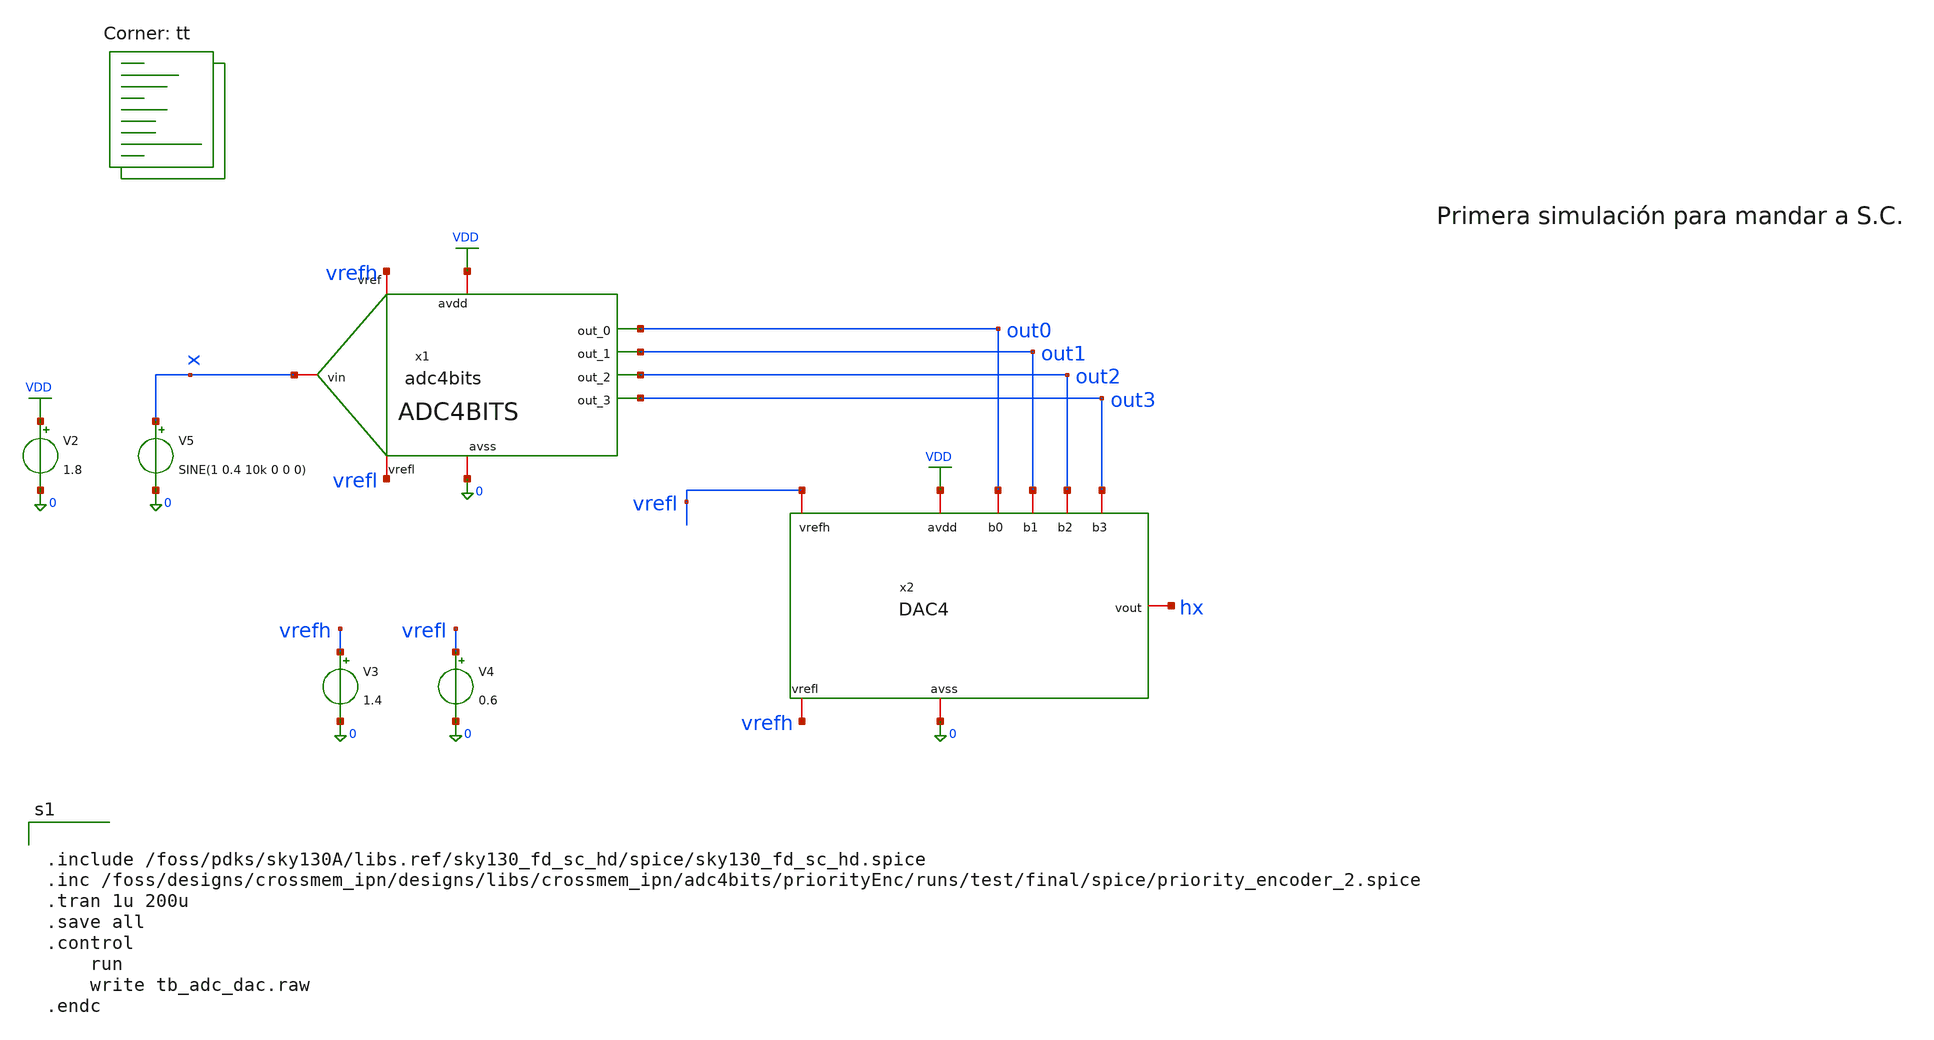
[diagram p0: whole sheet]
** sch_path: designs/libs/crossmem_ipn/tb_adc_dac.sch
**.subckt tb_adc_dac
x1 x vrefh out0 out1 out2 out3 0 VDD vrefl adc4bits
V2 VDD 0 1.8
x2 VDD out0 out1 0 out2 vrefl hx vrefh out3 DAC4
V3 vrefh 0 1.4
V4 vrefl 0 0.6
V5 x 0 SINE(1 0.4 10k 0 0 0)
**** begin user architecture code


.include /foss/pdks/sky130A/libs.ref/sky130_fd_sc_hd/spice/sky130_fd_sc_hd.spice
.inc /foss/designs/crossmem_ipn/designs/libs/crossmem_ipn/adc4bits/priorityEnc/runs/test/final/spice/priority_encoder_2.spice
.tran 1u 200u
.save all
.control
	run
	write tb_adc_dac.raw
.endc


.lib $::SKYWATER_MODELS/sky130.lib.spice tt
**** end user architecture code
**.ends

* expanding   symbol:  /foss/designs/crossmem_ipn/designs/libs/crossmem_ipn/adc4bits/adc4bits.sym #
*+ of pins=9
** sym_path: designs/libs/crossmem_ipn/adc4bits/adc4bits.sym
** sch_path: designs/libs/crossmem_ipn/adc4bits/adc4bits.sch
.subckt adc4bits vin vref out_0 out_1 out_2 out_3 avss avdd vrefl
*.iopin vref
*.iopin avss
*.iopin vin
*.opin out_0
*.opin out_1
*.opin out_2
*.opin out_3
*.iopin avdd
*.iopin vrefl
x1 avdd vin vref n1 avss opamp
x2 avdd vin v1 n2 avss opamp
x3 avdd vin v2 n3 avss opamp
x4 avdd vin v3 n4 avss opamp
x5 avdd vin v4 n5 avss opamp
x6 avdd vin v5 n6 avss opamp
x7 avdd vin v6 n7 avss opamp
x8 avdd vin v7 n8 avss opamp
x9 avdd vin v8 n9 avss opamp
x10 avdd vin v9 n10 avss opamp
x11 avdd vin v10 n11 avss opamp
x12 avdd vin v11 n12 avss opamp
x13 avdd vin v12 n13 avss opamp
x14 avdd vin v13 n14 avss opamp
x15 avdd vin v14 n15 avss opamp
x16 avss avdd n1 n11 n12 n13 n14 n15 avss n2 n3 n4 n5 n6 n7 n8 n9 n10 out_0 out_1 out_2 out_3
+ priority_encoder
R1 v1 vref sky130_fd_pr__res_generic_l1 W=1 L=3.75 m=1
R2 v2 v1 sky130_fd_pr__res_generic_l1 W=1 L=3.75 m=1
R3 v3 v2 sky130_fd_pr__res_generic_l1 W=1 L=3.75 m=1
R4 v4 v3 sky130_fd_pr__res_generic_l1 W=1 L=3.75 m=1
R5 v5 v4 sky130_fd_pr__res_generic_l1 W=1 L=3.75 m=1
R6 v6 v5 sky130_fd_pr__res_generic_l1 W=1 L=3.75 m=1
R7 v7 v6 sky130_fd_pr__res_generic_l1 W=1 L=3.75 m=1
R8 v8 v7 sky130_fd_pr__res_generic_l1 W=1 L=3.75 m=1
R9 v9 v8 sky130_fd_pr__res_generic_l1 W=1 L=3.75 m=1
R10 v10 v9 sky130_fd_pr__res_generic_l1 W=1 L=3.75 m=1
R11 v11 v10 sky130_fd_pr__res_generic_l1 W=1 L=3.75 m=1
R12 v12 v11 sky130_fd_pr__res_generic_l1 W=1 L=3.75 m=1
R13 v13 v12 sky130_fd_pr__res_generic_l1 W=1 L=3.75 m=1
R14 v14 v13 sky130_fd_pr__res_generic_l1 W=1 L=3.75 m=1
R15 vrefl v14 sky130_fd_pr__res_generic_l1 W=1 L=3.75 m=1
.ends


* expanding   symbol:  /foss/designs/crossmem_ipn/designs/libs/crossmem_ipn/dac4bits/sch/DAC4.sym #
*+ of pins=9
** sym_path: designs/libs/crossmem_ipn/dac4bits/sch/DAC4.sym
** sch_path: designs/libs/crossmem_ipn/dac4bits/sch/DAC4.sch
.subckt DAC4 avdd b0 b1 avss b2 vrefh vout vrefl b3
*.iopin avdd
*.iopin avss
*.iopin b0
*.iopin b1
*.iopin b2
*.iopin vout
*.iopin b3
*.iopin vrefh
*.iopin vrefl
x1 avdd b0 b1 avss b2 vrefh net2 net1 DAC3
x2 avdd b0 b1 avss b2 net1 net3 vrefl DAC3
x3 avdd b3 avss net2 vout net3 sw
.ends


* expanding   symbol:  /foss/designs/crossmem_ipn/designs/libs/crossmem_ipn/opamp/opamp.sym # of
*+ pins=5
** sym_path: designs/libs/crossmem_ipn/opamp/opamp.sym
** sch_path: designs/libs/crossmem_ipn/opamp/opamp.sch
.subckt opamp vdd vin1 vin2 vout vss
*.iopin vss
*.iopin vdd
*.opin vout
*.ipin vin1
*.ipin vin2
XM3 net1 net1 vdd vdd sky130_fd_pr__pfet_01v8 L=1 W=9 nf=1 ad='int((1 + 1)/2) * 9 / 1 * 0.29' as='int((1 + 2)/2) * 9 / 1 * 0.29'
+ pd='2*int((1 + 1)/2) * (9 / 1 + 0.29)' ps='2*int((1 + 2)/2) * (9 / 1 + 0.29)' nrd='0.29 / 9 ' nrs='0.29 / 9 '
+ sa=0 sb=0 sd=0 mult=1 m=1
XM4 net2 net1 vdd vdd sky130_fd_pr__pfet_01v8 L=1 W=9 nf=1 ad='int((1 + 1)/2) * 9 / 1 * 0.29' as='int((1 + 2)/2) * 9 / 1 * 0.29'
+ pd='2*int((1 + 1)/2) * (9 / 1 + 0.29)' ps='2*int((1 + 2)/2) * (9 / 1 + 0.29)' nrd='0.29 / 9 ' nrs='0.29 / 9 '
+ sa=0 sb=0 sd=0 mult=1 m=1
XM6 vout net2 vdd vdd sky130_fd_pr__pfet_01v8 L=1 W=8.65 nf=20 ad='int((20 + 1)/2) * 8.65 / 20 * 0.29'
+ as='int((20 + 2)/2) * 8.65 / 20 * 0.29' pd='2*int((20 + 1)/2) * (8.65 / 20 + 0.29)' ps='2*int((20 + 2)/2) * (8.65 / 20 + 0.29)'
+ nrd='0.29 / 8.65 ' nrs='0.29 / 8.65 ' sa=0 sb=0 sd=0 mult=1 m=1
XM1 net1 vin1 net3 vss sky130_fd_pr__nfet_01v8 L=1 W=5 nf=1 ad='int((1 + 1)/2) * 5 / 1 * 0.29' as='int((1 + 2)/2) * 5 / 1 * 0.29'
+ pd='2*int((1 + 1)/2) * (5 / 1 + 0.29)' ps='2*int((1 + 2)/2) * (5 / 1 + 0.29)' nrd='0.29 / 5 ' nrs='0.29 / 5 '
+ sa=0 sb=0 sd=0 mult=1 m=1
XM2 net2 vin2 net3 vss sky130_fd_pr__nfet_01v8 L=1 W=5 nf=1 ad='int((1 + 1)/2) * 5 / 1 * 0.29' as='int((1 + 2)/2) * 5 / 1 * 0.29'
+ pd='2*int((1 + 1)/2) * (5 / 1 + 0.29)' ps='2*int((1 + 2)/2) * (5 / 1 + 0.29)' nrd='0.29 / 5 ' nrs='0.29 / 5 '
+ sa=0 sb=0 sd=0 mult=1 m=1
XM5 net3 vb1 vss vss sky130_fd_pr__nfet_01v8 L=1 W=8 nf=1 ad='int((1 + 1)/2) * 8 / 1 * 0.29' as='int((1 + 2)/2) * 8 / 1 * 0.29'
+ pd='2*int((1 + 1)/2) * (8 / 1 + 0.29)' ps='2*int((1 + 2)/2) * (8 / 1 + 0.29)' nrd='0.29 / 8 ' nrs='0.29 / 8 '
+ sa=0 sb=0 sd=0 mult=1 m=1
XM8 vb1 vb1 vss vss sky130_fd_pr__nfet_01v8 L=1 W=8 nf=1 ad='int((1 + 1)/2) * 8 / 1 * 0.29' as='int((1 + 2)/2) * 8 / 1 * 0.29'
+ pd='2*int((1 + 1)/2) * (8 / 1 + 0.29)' ps='2*int((1 + 2)/2) * (8 / 1 + 0.29)' nrd='0.29 / 8 ' nrs='0.29 / 8 '
+ sa=0 sb=0 sd=0 mult=1 m=1
XM7 vout vb1 vss vss sky130_fd_pr__nfet_01v8 L=1 W=7 nf=16 ad='int((16 + 1)/2) * 7 / 16 * 0.29' as='int((16 + 2)/2) * 7 / 16 * 0.29'
+ pd='2*int((16 + 1)/2) * (7 / 16 + 0.29)' ps='2*int((16 + 2)/2) * (7 / 16 + 0.29)' nrd='0.29 / 7 ' nrs='0.29 / 7 '
+ sa=0 sb=0 sd=0 mult=1 m=1
XC1 net2 vout sky130_fd_pr__cap_mim_m3_1 W=30 L=30 MF=1 m=1
XM9 vb1 vb1 vdd vdd sky130_fd_pr__pfet_01v8 L=0.5 W=0.5 nf=1 ad='int((1 + 1)/2) * 0.5 / 1 * 0.29' as='int((1 + 2)/2) * 0.5 / 1 * 0.29'
+ pd='2*int((1 + 1)/2) * (0.5 / 1 + 0.29)' ps='2*int((1 + 2)/2) * (0.5 / 1 + 0.29)' nrd='0.29 / 0.5 ' nrs='0.29 / 0.5 '
+ sa=0 sb=0 sd=0 mult=1 m=1
.ends


* expanding   symbol:  /foss/designs/crossmem_ipn/designs/libs/crossmem_ipn/dac4bits/sch/DAC3.sym #
*+ of pins=8
** sym_path: designs/libs/crossmem_ipn/dac4bits/sch/DAC3.sym
** sch_path: designs/libs/crossmem_ipn/dac4bits/sch/DAC3.sch
.subckt DAC3 avdd b0 b1 avss b2 vrefh vout vrefl
*.iopin vrefh
*.iopin vrefl
*.iopin b0
*.iopin b1
*.iopin b2
*.iopin avdd
*.iopin avss
*.iopin vout
x1 b0 avdd b1 avss vrefh net1 net3 DAC2BIT
x2 b0 avdd b1 avss net3 net2 vrefl DAC2BIT
x3 avdd b2 avss net1 vout net2 sw
.ends


* expanding   symbol:  /foss/designs/crossmem_ipn/designs/libs/crossmem_ipn/dac4bits/sch/sw.sym # of
*+ pins=6
** sym_path: designs/libs/crossmem_ipn/dac4bits/sch/sw.sym
** sch_path: designs/libs/crossmem_ipn/dac4bits/sch/sw.sch
.subckt sw avdd b_in avss vin1 vout vin2
*.iopin avss
*.iopin vin1
*.iopin vout
*.iopin avdd
*.iopin vin2
*.iopin b_in
XM1 net1 b_in avss avss sky130_fd_pr__nfet_01v8 L=0.15 W=0.5 nf=1 ad='int((nf+1)/2) * W/nf * 0.29' as='int((nf+2)/2) * W/nf * 0.29'
+ pd='2*int((nf+1)/2) * (W/nf + 0.29)' ps='2*int((nf+2)/2) * (W/nf + 0.29)' nrd='0.29 / W' nrs='0.29 / W'
+ sa=0 sb=0 sd=0 mult=1 m=1
XM2 net1 b_in avdd avdd sky130_fd_pr__pfet_01v8 L=0.15 W=0.5 nf=1 ad='int((nf+1)/2) * W/nf * 0.29' as='int((nf+2)/2) * W/nf * 0.29'
+ pd='2*int((nf+1)/2) * (W/nf + 0.29)' ps='2*int((nf+2)/2) * (W/nf + 0.29)' nrd='0.29 / W' nrs='0.29 / W'
+ sa=0 sb=0 sd=0 mult=1 m=1
XM3 net2 net1 avss avss sky130_fd_pr__nfet_01v8 L=0.15 W=0.5 nf=1 ad='int((nf+1)/2) * W/nf * 0.29' as='int((nf+2)/2) * W/nf * 0.29'
+ pd='2*int((nf+1)/2) * (W/nf + 0.29)' ps='2*int((nf+2)/2) * (W/nf + 0.29)' nrd='0.29 / W' nrs='0.29 / W'
+ sa=0 sb=0 sd=0 mult=1 m=1
XM4 net2 net1 avdd avdd sky130_fd_pr__pfet_01v8 L=0.15 W=0.5 nf=1 ad='int((nf+1)/2) * W/nf * 0.29' as='int((nf+2)/2) * W/nf * 0.29'
+ pd='2*int((nf+1)/2) * (W/nf + 0.29)' ps='2*int((nf+2)/2) * (W/nf + 0.29)' nrd='0.29 / W' nrs='0.29 / W'
+ sa=0 sb=0 sd=0 mult=1 m=1
XM5 vout net1 vin1 avdd sky130_fd_pr__pfet_01v8 L=0.15 W=0.5 nf=1 ad='int((nf+1)/2) * W/nf * 0.29' as='int((nf+2)/2) * W/nf * 0.29'
+ pd='2*int((nf+1)/2) * (W/nf + 0.29)' ps='2*int((nf+2)/2) * (W/nf + 0.29)' nrd='0.29 / W' nrs='0.29 / W'
+ sa=0 sb=0 sd=0 mult=1 m=1
XM6 vout net1 vin2 avss sky130_fd_pr__nfet_01v8 L=0.15 W=0.5 nf=1 ad='int((nf+1)/2) * W/nf * 0.29' as='int((nf+2)/2) * W/nf * 0.29'
+ pd='2*int((nf+1)/2) * (W/nf + 0.29)' ps='2*int((nf+2)/2) * (W/nf + 0.29)' nrd='0.29 / W' nrs='0.29 / W'
+ sa=0 sb=0 sd=0 mult=1 m=1
XM7 vin1 net2 vout avss sky130_fd_pr__nfet_01v8 L=0.15 W=0.5 nf=1 ad='int((nf+1)/2) * W/nf * 0.29' as='int((nf+2)/2) * W/nf * 0.29'
+ pd='2*int((nf+1)/2) * (W/nf + 0.29)' ps='2*int((nf+2)/2) * (W/nf + 0.29)' nrd='0.29 / W' nrs='0.29 / W'
+ sa=0 sb=0 sd=0 mult=1 m=1
XM8 vin2 net2 vout avdd sky130_fd_pr__pfet_01v8 L=0.15 W=0.5 nf=1 ad='int((nf+1)/2) * W/nf * 0.29' as='int((nf+2)/2) * W/nf * 0.29'
+ pd='2*int((nf+1)/2) * (W/nf + 0.29)' ps='2*int((nf+2)/2) * (W/nf + 0.29)' nrd='0.29 / W' nrs='0.29 / W'
+ sa=0 sb=0 sd=0 mult=1 m=1
.ends


* expanding   symbol:  /foss/designs/crossmem_ipn/designs/libs/crossmem_ipn/dac4bits/sch/DAC2BIT.sym
*+ # of pins=7
** sym_path: designs/libs/crossmem_ipn/dac4bits/sch/DAC2BIT.sym
** sch_path: designs/libs/crossmem_ipn/dac4bits/sch/DAC2BIT.sch
.subckt DAC2BIT b0 avdd b1 avss vrefh vout vrefl
*.iopin vrefh
*.iopin vrefl
*.iopin b0
*.iopin b1
*.iopin avdd
*.iopin avss
*.iopin vout
x1 avdd b0 avss net5 net1 net4 sw
x2 avdd b0 avss net3 net2 vrefl sw
x3 avdd b1 avss net1 vout net2 sw
R5 net5 vrefh sky130_fd_pr__res_generic_l1 W=1 L=3.75 m=1
R6 net4 net5 sky130_fd_pr__res_generic_l1 W=1 L=3.75 m=1
R7 net3 net4 sky130_fd_pr__res_generic_l1 W=1 L=3.75 m=1
R8 vrefl net3 sky130_fd_pr__res_generic_l1 W=1 L=3.75 m=1
.ends

.GLOBAL VDD
.end
